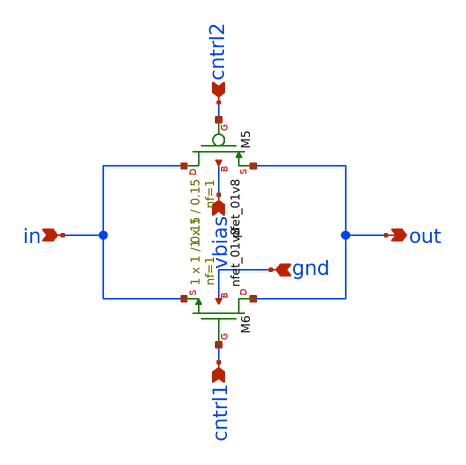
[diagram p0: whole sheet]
** sch_path: xschem/attenuator/gate-switch.sch
**.subckt gate-switch in vbias gnd out cntrl1 cntrl2
*.ipin in
*.ipin vbias
*.ipin gnd
*.opin out
*.ipin cntrl1
*.ipin cntrl2
XM5 in cntrl2 out vbias sky130_fd_pr__pfet_01v8 L=0.15 W=1 nf=1 ad='int((nf+1)/2) * W/nf * 0.29' as='int((nf+2)/2) * W/nf * 0.29'
+ pd='2*int((nf+1)/2) * (W/nf + 0.29)' ps='2*int((nf+2)/2) * (W/nf + 0.29)' nrd='0.29 / W' nrs='0.29 / W'
+ sa=0 sb=0 sd=0 mult=1 m=1
XM6 out cntrl1 in gnd sky130_fd_pr__nfet_01v8 L=0.15 W=1 nf=1 ad='int((nf+1)/2) * W/nf * 0.29' as='int((nf+2)/2) * W/nf * 0.29'
+ pd='2*int((nf+1)/2) * (W/nf + 0.29)' ps='2*int((nf+2)/2) * (W/nf + 0.29)' nrd='0.29 / W' nrs='0.29 / W'
+ sa=0 sb=0 sd=0 mult=1 m=1
**.ends
.end
